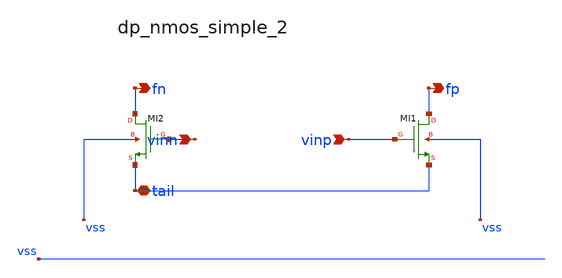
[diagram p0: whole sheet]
** sch_path: analog-db/raw/amp_023_fer_fd2s/hier/blocks/dp_nmos_simple_2.sch
**.subckt dp_nmos_simple_2 vinn vinp tail fn fp
*.ipin vinn
*.ipin vinp
*.iopin tail
*.opin fn
*.opin fp
XMI1 fp vinp tail vss sg13_lv_nmos w=x_dut_xmi1_w l=x_dut_xmi1_l ng=1 m=x_dut_xmi1_m
XMI2 fn vinn tail vss sg13_lv_nmos w=x_dut_xmi2_w l=x_dut_xmi2_l ng=1 m=x_dut_xmi2_m
**.ends
.end
